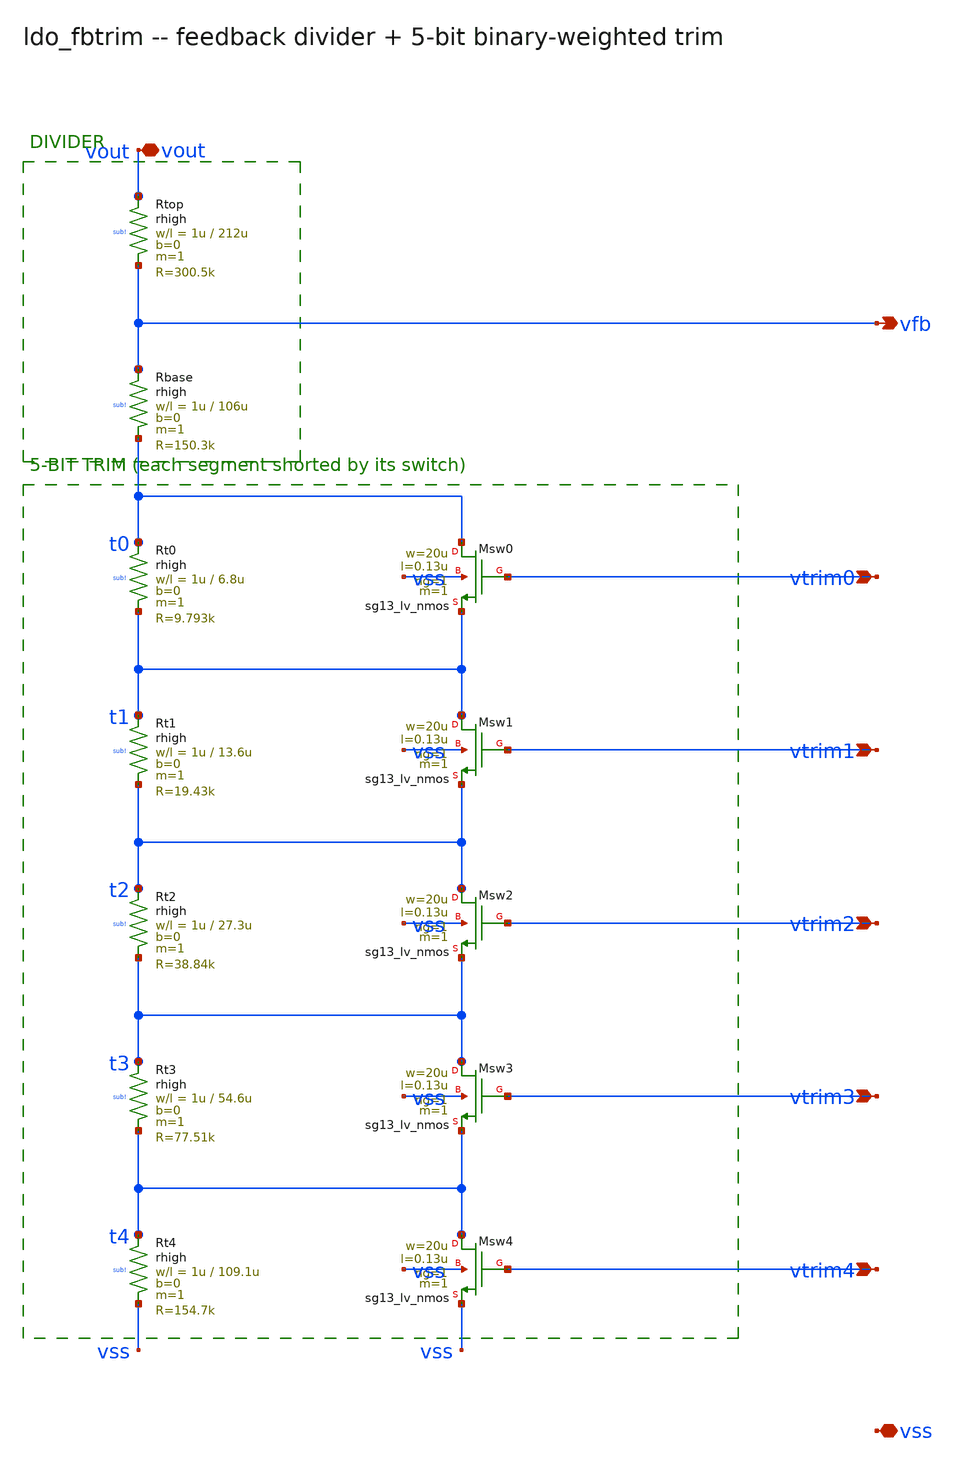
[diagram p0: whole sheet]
** sch_path: xschem/ldo_fbtrim.sch
**.subckt ldo_fbtrim vout vfb vss vtrim0 vtrim1 vtrim2 vtrim3 vtrim4
*.iopin vout
*.opin vfb
*.iopin vss
*.ipin vtrim0
*.ipin vtrim1
*.ipin vtrim2
*.ipin vtrim3
*.ipin vtrim4
XRtop vout vfb sub! rhigh w=1u l=212u m=1 b=0 mm_ok=1
XRbase vfb t0 sub! rhigh w=1u l=106u m=1 b=0 mm_ok=1
XRt0 t0 t1 sub! rhigh w=1u l=6.8u m=1 b=0 mm_ok=1
XMsw0 t0 vtrim0 t1 vss sg13_lv_nmos w=20u l=0.13u ng=1 m=1 mm_ok=1
XRt1 t1 t2 sub! rhigh w=1u l=13.6u m=1 b=0 mm_ok=1
XMsw1 t1 vtrim1 t2 vss sg13_lv_nmos w=20u l=0.13u ng=1 m=1 mm_ok=1
XRt2 t2 t3 sub! rhigh w=1u l=27.3u m=1 b=0 mm_ok=1
XMsw2 t2 vtrim2 t3 vss sg13_lv_nmos w=20u l=0.13u ng=1 m=1 mm_ok=1
XRt3 t3 t4 sub! rhigh w=1u l=54.6u m=1 b=0 mm_ok=1
XMsw3 t3 vtrim3 t4 vss sg13_lv_nmos w=20u l=0.13u ng=1 m=1 mm_ok=1
XRt4 t4 vss sub! rhigh w=1u l=109.1u m=1 b=0 mm_ok=1
XMsw4 t4 vtrim4 vss vss sg13_lv_nmos w=20u l=0.13u ng=1 m=1 mm_ok=1
**.ends
.end
